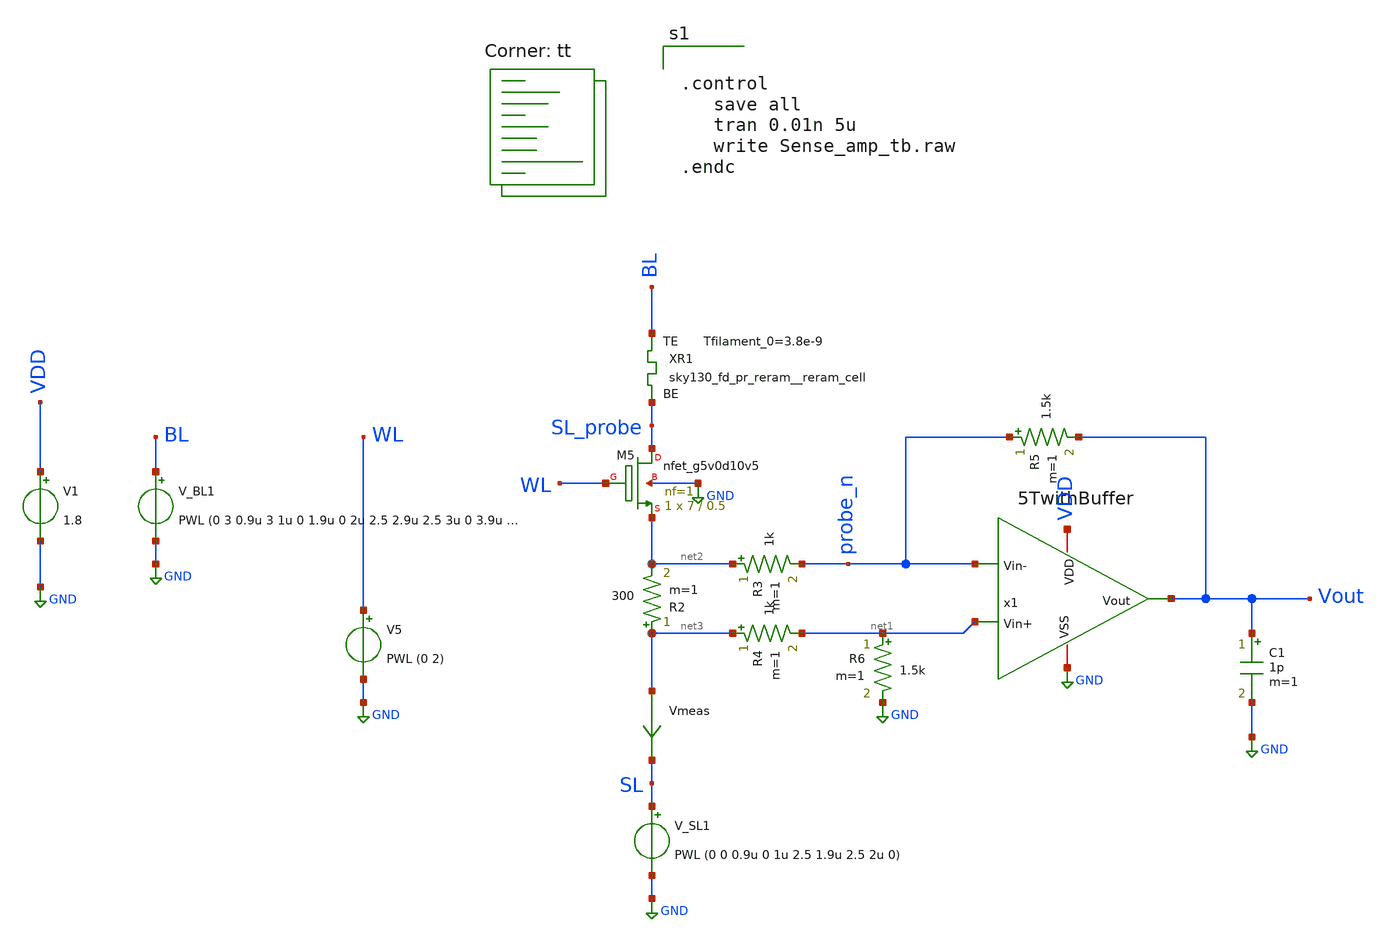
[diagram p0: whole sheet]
** sch_path: xschem/test/xschem/Sense_amp_tb.sch
* StefanSchippers/xschem_sky130/sky130_fd_pr/reram.sym:
* Copyright 2021 Stefan Frederik Schippers
* Licensed under the Apache License, Version 2.0 (the "License");
**.subckt Sense_amp_tb
V1 VDD GND 1.8
XR1 BL SL_probe sky130_fd_pr_reram__reram_cell Tfilament_0=3.8e-9
XM5 SL_probe WL net2 GND sky130_fd_pr__nfet_g5v0d10v5 L=0.5 W=7 nf=1 ad='int((nf+1)/2) * W/nf * 0.29'
+ as='int((nf+2)/2) * W/nf * 0.29' pd='2*int((nf+1)/2) * (W/nf + 0.29)' ps='2*int((nf+2)/2) * (W/nf + 0.29)'
+ nrd='0.29 / W' nrs='0.29 / W' sa=0 sb=0 sd=0 mult=1 m=1
V_BL1 BL GND PWL (0 3 0.9u 3 1u 0 1.9u 0 2u 2.5 2.9u 2.5 3u 0 3.9u 0 4u 0.2)
V_SL1 SL GND PWL (0 0 0.9u 0 1u 2.5 1.9u 2.5 2u 0)
V5 WL GND PWL (0 2)
x1 VDD Vout probe_n net1 GND 5TwithBuffer
R2 net3 net2 300 m=1
C1 Vout GND 1p m=1
Vmeas net3 SL 0
.save i(vmeas)
R3 net2 probe_n 1k m=1
R4 net3 net1 1k m=1
R5 probe_n Vout 1.5k m=1
R6 net1 GND 1.5k m=1
**** begin user architecture code
.lib $::SKYWATER_MODELS/sky130.lib.spice tt


.control
   save all
   tran 0.01n 5u
   write Sense_amp_tb.raw
.endc


**** end user architecture code
**.ends

* expanding   symbol:  amplifiers/dec24/5TwithBuffer.sym # of pins=5
** sym_path: amplifiers/dec24/5TwithBuffer.sym
** sch_path: amplifiers/dec24/5TwithBuffer.sch
.subckt 5TwithBuffer VDD Vout Vin- Vin+ VSS
*.iopin VDD
*.iopin VSS
*.ipin Vin-
*.ipin Vin+
*.opin Vout
I0 VDD Vb1 100u
XM1 net1 Vin+ Vsink VSS sky130_fd_pr__nfet_01v8 L=1 W=4 nf=1 ad='int((nf+1)/2) * W/nf * 0.29' as='int((nf+2)/2) * W/nf * 0.29'
+ pd='2*int((nf+1)/2) * (W/nf + 0.29)' ps='2*int((nf+2)/2) * (W/nf + 0.29)' nrd='0.29 / W' nrs='0.29 / W'
+ sa=0 sb=0 sd=0 mult=1 m=1
XM2 Vout Vin- Vsink VSS sky130_fd_pr__nfet_01v8 L=1 W=4 nf=1 ad='int((nf+1)/2) * W/nf * 0.29' as='int((nf+2)/2) * W/nf * 0.29'
+ pd='2*int((nf+1)/2) * (W/nf + 0.29)' ps='2*int((nf+2)/2) * (W/nf + 0.29)' nrd='0.29 / W' nrs='0.29 / W'
+ sa=0 sb=0 sd=0 mult=1 m=1
XM3 Vb1 Vb1 VSS VSS sky130_fd_pr__nfet_01v8 L=1 W=5 nf=1 ad='int((nf+1)/2) * W/nf * 0.29' as='int((nf+2)/2) * W/nf * 0.29'
+ pd='2*int((nf+1)/2) * (W/nf + 0.29)' ps='2*int((nf+2)/2) * (W/nf + 0.29)' nrd='0.29 / W' nrs='0.29 / W'
+ sa=0 sb=0 sd=0 mult=1 m=1
XM4 Vsink Vb1 VSS VSS sky130_fd_pr__nfet_01v8 L=1 W=5 nf=1 ad='int((nf+1)/2) * W/nf * 0.29' as='int((nf+2)/2) * W/nf * 0.29'
+ pd='2*int((nf+1)/2) * (W/nf + 0.29)' ps='2*int((nf+2)/2) * (W/nf + 0.29)' nrd='0.29 / W' nrs='0.29 / W'
+ sa=0 sb=0 sd=0 mult=1 m=1
XM7 VDD Vout net2 VSS sky130_fd_pr__nfet_01v8 L=1 W=20 nf=1 ad='int((nf+1)/2) * W/nf * 0.29' as='int((nf+2)/2) * W/nf * 0.29'
+ pd='2*int((nf+1)/2) * (W/nf + 0.29)' ps='2*int((nf+2)/2) * (W/nf + 0.29)' nrd='0.29 / W' nrs='0.29 / W'
+ sa=0 sb=0 sd=0 mult=1 m=1
XM8 net2 Vb1 VSS VSS sky130_fd_pr__nfet_01v8 L=1 W=5 nf=1 ad='int((nf+1)/2) * W/nf * 0.29' as='int((nf+2)/2) * W/nf * 0.29'
+ pd='2*int((nf+1)/2) * (W/nf + 0.29)' ps='2*int((nf+2)/2) * (W/nf + 0.29)' nrd='0.29 / W' nrs='0.29 / W'
+ sa=0 sb=0 sd=0 mult=5 m=5
XM5 net1 net1 VDD VDD sky130_fd_pr__pfet_01v8_lvt L=1 W=10 nf=1 ad='int((nf+1)/2) * W/nf * 0.29' as='int((nf+2)/2) * W/nf * 0.29'
+ pd='2*int((nf+1)/2) * (W/nf + 0.29)' ps='2*int((nf+2)/2) * (W/nf + 0.29)' nrd='0.29 / W' nrs='0.29 / W'
+ sa=0 sb=0 sd=0 mult=1 m=1
XM6 VDD net1 Vout VDD sky130_fd_pr__pfet_01v8_lvt L=1 W=10 nf=1 ad='int((nf+1)/2) * W/nf * 0.29' as='int((nf+2)/2) * W/nf * 0.29'
+ pd='2*int((nf+1)/2) * (W/nf + 0.29)' ps='2*int((nf+2)/2) * (W/nf + 0.29)' nrd='0.29 / W' nrs='0.29 / W'
+ sa=0 sb=0 sd=0 mult=1 m=1
.ends

.GLOBAL GND
.GLOBAL VDD
**** begin user architecture code

.subckt sky130_fd_pr_reram__reram_cell TE BE Tfilament_0=3.3e-9 area_ox=0.1024e-12
N1 TE BE nFilament sky130_fd_pr_reram__reram_model
.ic v(nFilament)={Tfilament_0*1.0e9}
.ends sky130_fd_pr_reram__reram_cell

.model sky130_fd_pr_reram__reram_model sky130_fd_pr_reram__reram_module  area_ox = 0.1024e-12  Tox =
+ 5.0  Tfilament_max = 4.9  Tfilament_min = 3.3  Eact_generation = 1.501  Eact_recombination  = 1.500
+  I_k1  = 6.140e-5  Tfilament_ref = 4.7249  V_ref = 0.430  velocity_k1 = 150  gamma_k0  = 16.5  gamma_k1
+  = -1.25  Temperature_0 = 300  C_thermal = 3.1825e-16  tau_thermal = 0.23e-9  t_step  = 1.0e-9
+  smoothing = 1e-7  Kclip = 200

.control
pre_osdi $SKYWATER_MODELS/sky130_fd_pr_reram__reram_module.osdi
.endc

**** end user architecture code
.end
